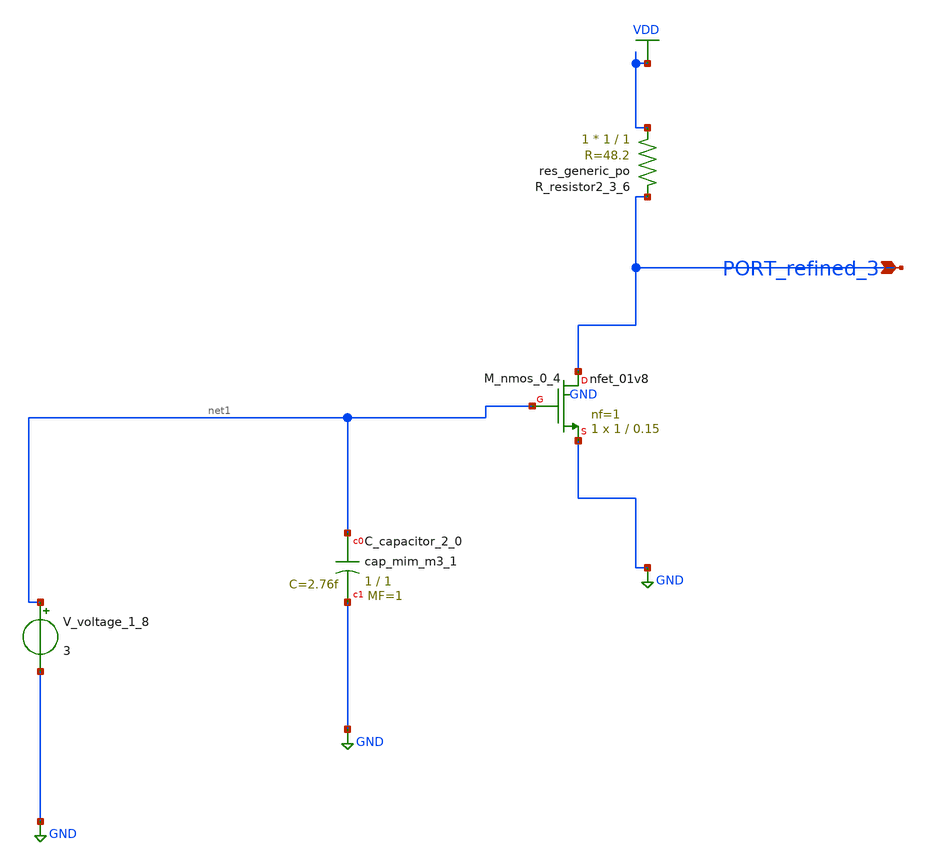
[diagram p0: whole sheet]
** sch_path: schematics/AMSNet/502.sch
**.subckt 502 PORT_refined_3
*.ipin PORT_refined_3
XC_capacitor_2_0 net1 GND sky130_fd_pr__cap_mim_m3_1 W=1 L=1 MF=1 m=1
XM_nmos_0_4 PORT_refined_3 net1 GND GND sky130_fd_pr__nfet_01v8 L=0.15 W=1 nf=1 ad='int((1 + 1)/2) * 1 / 1 * 0.29'
+ as='int((1 + 2)/2) * 1 / 1 * 0.29' pd='2*int((1 + 1)/2) * (1 / 1 + 0.29)' ps='2*int((1 + 2)/2) * (1 / 1 + 0.29)'
+ nrd='0.29 / 1 ' nrs='0.29 / 1 ' sa=0 sb=0 sd=0 mult=1 m=1
XR_resistor2_3_6 VDD PORT_refined_3 sky130_fd_pr__res_generic_po W=1 L=1 m=1
V_voltage_1_8 net1 GND 3
**.ends
.GLOBAL GND
.GLOBAL VDD
.end
